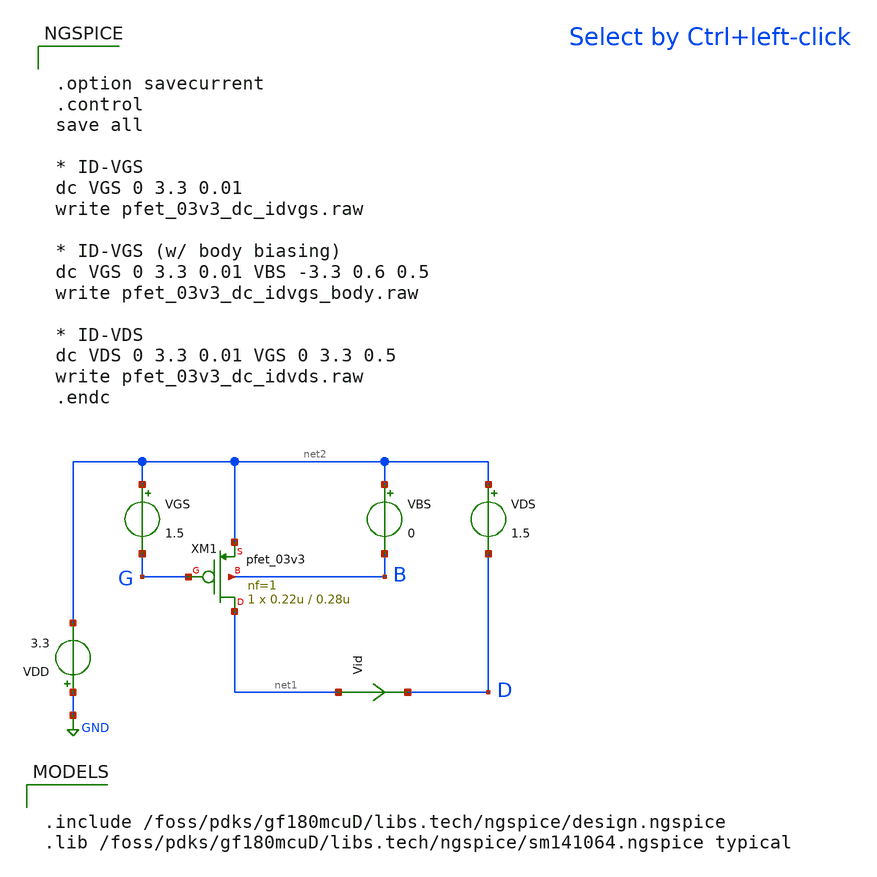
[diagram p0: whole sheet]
** sch_path: mosfet_gf180/pfet_03v3_dc.sch
**.subckt pfet_03v3_dc
VBS net2 B 0
VGS net2 G 1.5
VDS net2 D 1.5
Vid net1 D 0
.save i(vid)
XM1 net1 G net2 B pfet_03v3 L=0.28u W=0.22u nf=1 ad='int((nf+1)/2) * W/nf * 0.18u' as='int((nf+2)/2) * W/nf * 0.18u'
+ pd='2*int((nf+1)/2) * (W/nf + 0.18u)' ps='2*int((nf+2)/2) * (W/nf + 0.18u)' nrd='0.18u / W' nrs='0.18u / W'
+ sa=0 sb=0 sd=0 m=1
VDD GND net2 3.3
**** begin user architecture code

.include /foss/pdks/gf180mcuD/libs.tech/ngspice/design.ngspice
.lib /foss/pdks/gf180mcuD/libs.tech/ngspice/sm141064.ngspice typical


.option savecurrent
.control
save all

* ID-VGS
dc VGS 0 3.3 0.01
write pfet_03v3_dc_idvgs.raw

* ID-VGS (w/ body biasing)
dc VGS 0 3.3 0.01 VBS -3.3 0.6 0.5
write pfet_03v3_dc_idvgs_body.raw

* ID-VDS
dc VDS 0 3.3 0.01 VGS 0 3.3 0.5
write pfet_03v3_dc_idvds.raw
.endc

**** end user architecture code
**.ends
.GLOBAL GND
.end
